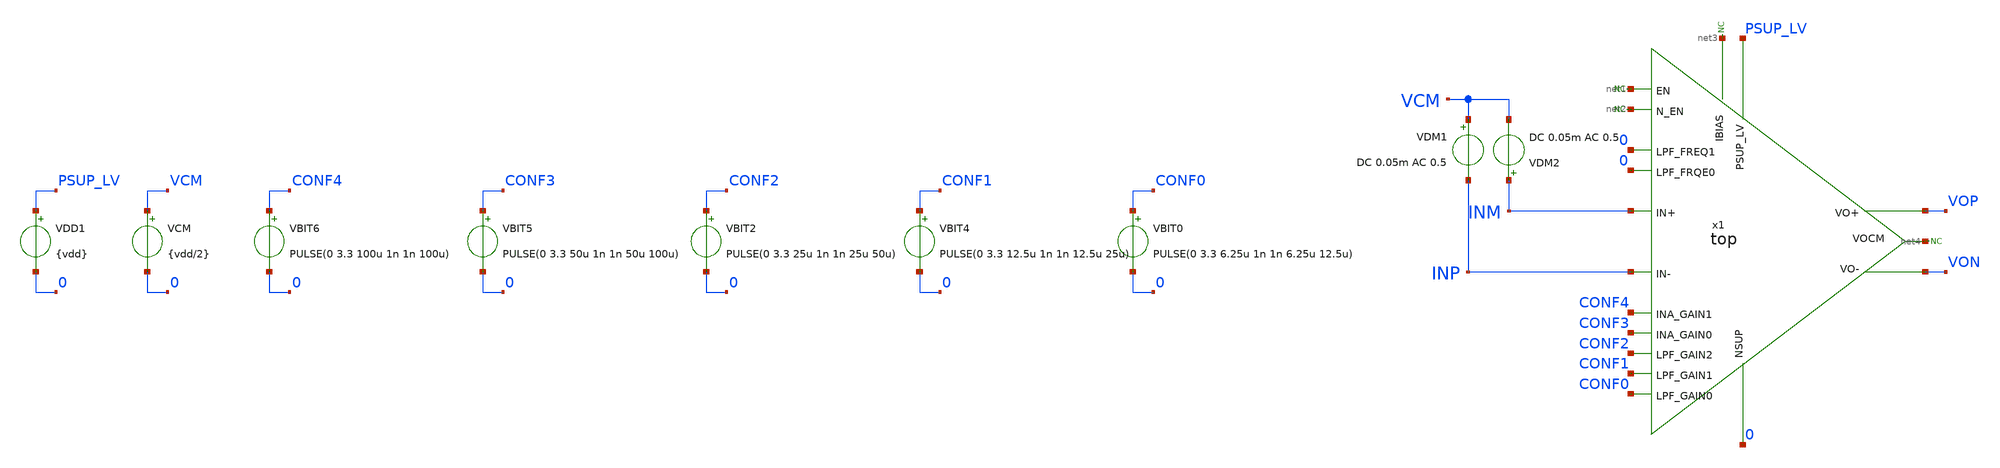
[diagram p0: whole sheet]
** sch_path: xschem/tb_top_tran.sch
**.subckt tb_top_tran
x1 PSUP_LV 0 net1 net2 net3 net4 CONF2 CONF1 CONF0 INM VOP INP VON 0 CONF4 0 CONF3 top
VBIT0 CONF0 0 PULSE(0 3.3 6.25u 1n 1n 6.25u 12.5u)
VBIT4 CONF1 0 PULSE(0 3.3 12.5u 1n 1n 12.5u 25u)
VCM VCM 0 {vdd/2}
VBIT2 CONF2 0 PULSE(0 3.3 25u 1n 1n 25u 50u)
VBIT5 CONF3 0 PULSE(0 3.3 50u 1n 1n 50u 100u)
VBIT6 CONF4 0 PULSE(0 3.3 100u 1n 1n 100u)
VDM2 INM VCM DC 0.05m AC 0.5
VDM1 VCM INP DC 0.05m AC 0.5
* noconn #net2
* noconn #net1
* noconn #net3
* noconn #net4
VDD1 PSUP_LV 0 {vdd}
**** begin user architecture code

.include $::180MCU_MODELS/design.ngspice

.lib $::180MCU_MODELS/sm141064.ngspice typical
.lib $::180MCU_MODELS/sm141064.ngspice res_typical
.lib $::180MCU_MODELS/sm141064.ngspice bjt_typical
.lib $::180MCU_MODELS/sm141064.ngspice mimcap_typical
.lib $::180MCU_MODELS/sm141064.ngspice cap_mim

.temp 25

.param vdd=3.3

* Deterministic PVT: disable random global/mismatch variation.
.param sw_stat_global=0
.param sw_stat_mismatch=0



.control
save all
tran 10n 200u

let Vid = v(INP) - v(INM)
let Vo = v(Vop) - v(Von)
let gain = v(Vo) / v(Vid)

write tb_top_tran.raw gain
.endc


**** end user architecture code
**.ends
.end
